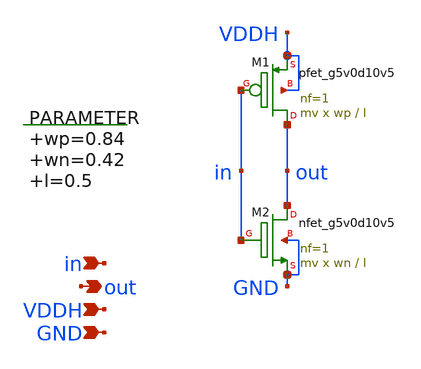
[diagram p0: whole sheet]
** sch_path: xschem/inv_hvl.sch
**.subckt inv_hvl out VDDH GND in
*.opin out
*.ipin VDDH
*.ipin GND
*.ipin in
.param wp=0.84 wn=0.42 l=0.5
XM1 out in VDDH VDDH sky130_fd_pr__pfet_g5v0d10v5 L=l W=wp nf=1 ad='int((nf+1)/2) * W/nf * 0.29' as='int((nf+2)/2) * W/nf * 0.29'
+ pd='2*int((nf+1)/2) * (W/nf + 0.29)' ps='2*int((nf+2)/2) * (W/nf + 0.29)' nrd='0.29 / W' nrs='0.29 / W'
+ sa=0 sb=0 sd=0 mult=mv m=mv
XM2 out in GND GND sky130_fd_pr__nfet_g5v0d10v5 L=l W=wn nf=1 ad='int((nf+1)/2) * W/nf * 0.29' as='int((nf+2)/2) * W/nf * 0.29'
+ pd='2*int((nf+1)/2) * (W/nf + 0.29)' ps='2*int((nf+2)/2) * (W/nf + 0.29)' nrd='0.29 / W' nrs='0.29 / W'
+ sa=0 sb=0 sd=0 mult=mv m=mv
**.ends
.end
